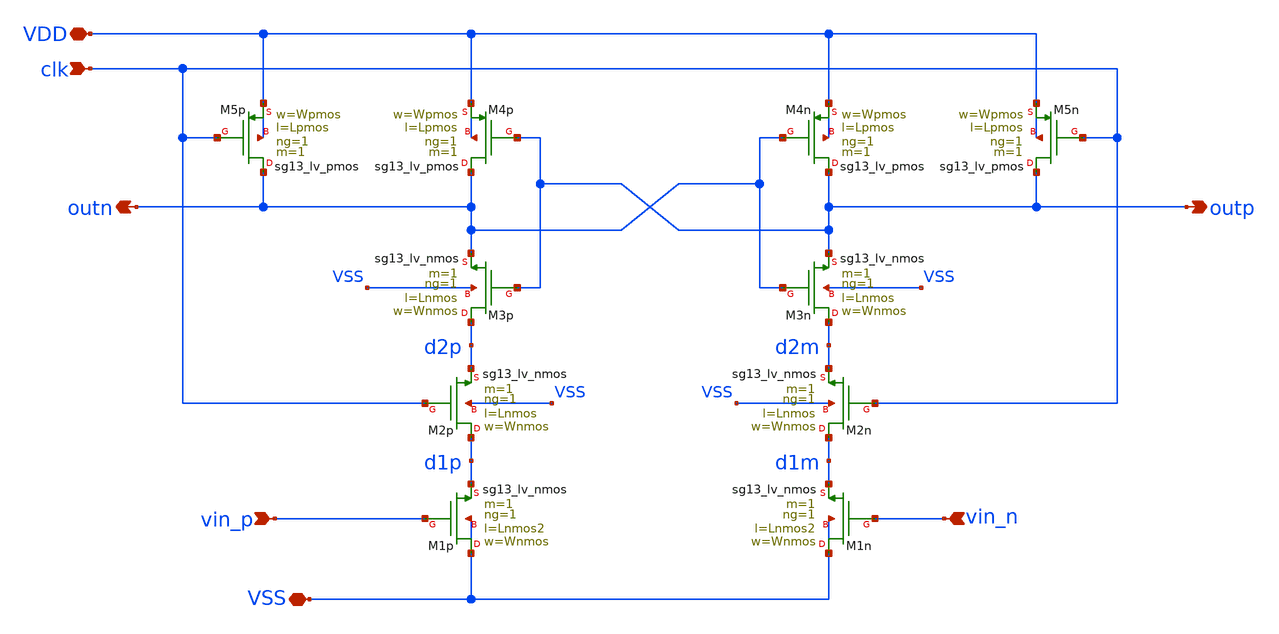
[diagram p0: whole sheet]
** sch_path: design/design_comp/comp_test.sch
**.subckt comp_test clk VSS VDD vin_n vin_p outn outp
*.ipin clk
*.iopin VSS
*.iopin VDD
*.ipin vin_n
*.ipin vin_p
*.opin outn
*.opin outp
XM5p outn clk VDD VDD sg13_lv_pmos w=Wpmos l=Lpmos ng=1 m=1 mm_ok=1
XM4n outp outn VDD VDD sg13_lv_pmos w=Wpmos l=Lpmos ng=1 m=1 mm_ok=1
XM4p outn outp VDD VDD sg13_lv_pmos w=Wpmos l=Lpmos ng=1 m=1 mm_ok=1
XM5n outp clk VDD VDD sg13_lv_pmos w=Wpmos l=Lpmos ng=1 m=1 mm_ok=1
XM3p d2p outp outn VSS sg13_lv_nmos w=Wnmos l=Lnmos ng=1 m=1 mm_ok=1
XM3n d2m outn outp VSS sg13_lv_nmos w=Wnmos l=Lnmos ng=1 m=1 mm_ok=1
XM2n d1m clk d2m VSS sg13_lv_nmos w=Wnmos l=Lnmos ng=1 m=1 mm_ok=1
XM2p d1p clk d2p VSS sg13_lv_nmos w=Wnmos l=Lnmos ng=1 m=1 mm_ok=1
XM1n VSS vin_n d1m VSS sg13_lv_nmos w=Wnmos l=Lnmos2 ng=1 m=1 mm_ok=1
XM1p VSS vin_p d1p VSS sg13_lv_nmos w=Wnmos l=Lnmos2 ng=1 m=1 mm_ok=1
**.ends
.end
